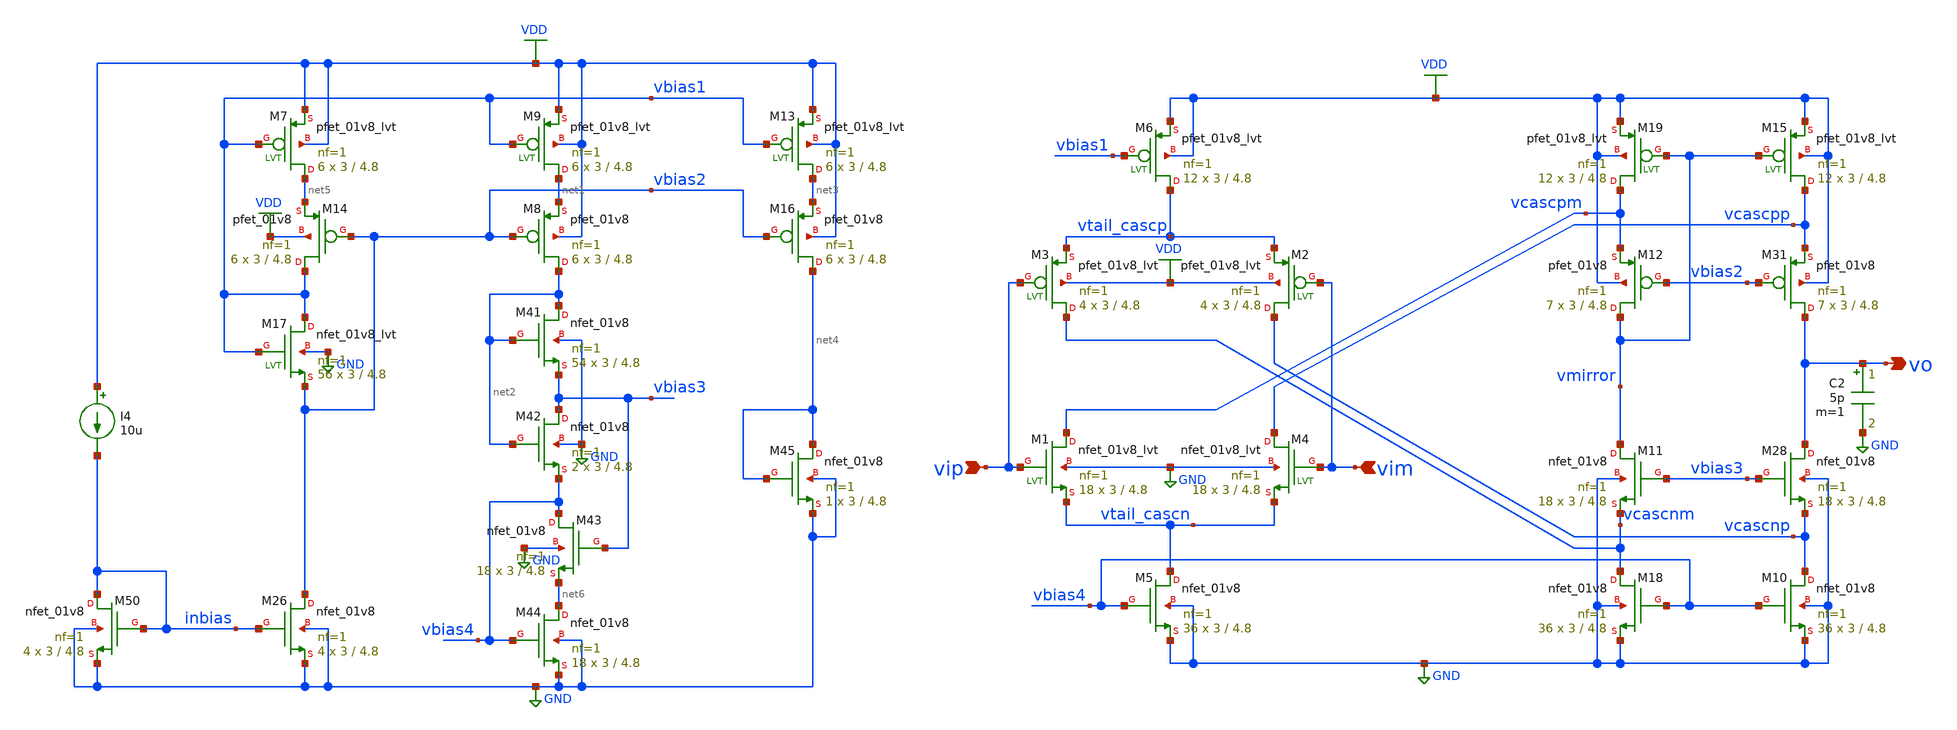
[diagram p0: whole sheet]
** sch_path: designs/se_fold_casc_wide_swing_ota_final.sch
* Copyright 2020 Stefan Frederik Schippers
* Licensed under the Apache License, Version 2.0 (the "License");
* you may not use this file except in compliance with the License.
* You may obtain a copy of the License at
* https://www.apache.org/licenses/LICENSE-2.0
* Unless required by applicable law or agreed to in writing, software
* distributed under the License is distributed on an "AS IS" BASIS,
* WITHOUT WARRANTIES OR CONDITIONS OF ANY KIND, either express or implied.
* See the License for the specific language governing permissions and
* limitations under the License.
**.subckt se_fold_casc_wide_swing_ota_final vip vim vo
*.ipin vip
*.ipin vim
*.opin vo
XM11 vmirror vbias3 vcascnm GND sky130_fd_pr__nfet_01v8 L=4.8 W=3 nf=1 ad='int((nf+1)/2) * W/nf * 0.29'
+ as='int((nf+2)/2) * W/nf * 0.29' pd='2*int((nf+1)/2) * (W/nf + 0.29)' ps='2*int((nf+2)/2) * (W/nf + 0.29)'
+ nrd='0.29 / W' nrs='0.29 / W' sa=0 sb=0 sd=0 mult=18 m=18
XM28 vo vbias3 vcascnp GND sky130_fd_pr__nfet_01v8 L=4.8 W=3 nf=1 ad='int((nf+1)/2) * W/nf * 0.29' as='int((nf+2)/2) * W/nf * 0.29'
+ pd='2*int((nf+1)/2) * (W/nf + 0.29)' ps='2*int((nf+2)/2) * (W/nf + 0.29)' nrd='0.29 / W' nrs='0.29 / W'
+ sa=0 sb=0 sd=0 mult=18 m=18
XM12 vmirror vbias2 vcascpm VDD sky130_fd_pr__pfet_01v8 L=4.8 W=3 nf=1 ad='int((nf+1)/2) * W/nf * 0.29'
+ as='int((nf+2)/2) * W/nf * 0.29' pd='2*int((nf+1)/2) * (W/nf + 0.29)' ps='2*int((nf+2)/2) * (W/nf + 0.29)'
+ nrd='0.29 / W' nrs='0.29 / W' sa=0 sb=0 sd=0 mult=7 m=7
XM31 vo vbias2 vcascpp VDD sky130_fd_pr__pfet_01v8 L=4.8 W=3 nf=1 ad='int((nf+1)/2) * W/nf * 0.29' as='int((nf+2)/2) * W/nf * 0.29'
+ pd='2*int((nf+1)/2) * (W/nf + 0.29)' ps='2*int((nf+2)/2) * (W/nf + 0.29)' nrd='0.29 / W' nrs='0.29 / W'
+ sa=0 sb=0 sd=0 mult=7 m=7
XM5 vtail_cascn vbias4 GND GND sky130_fd_pr__nfet_01v8 L=4.8 W=3 nf=1 ad='int((nf+1)/2) * W/nf * 0.29'
+ as='int((nf+2)/2) * W/nf * 0.29' pd='2*int((nf+1)/2) * (W/nf + 0.29)' ps='2*int((nf+2)/2) * (W/nf + 0.29)'
+ nrd='0.29 / W' nrs='0.29 / W' sa=0 sb=0 sd=0 mult=36 m=36
XM6 vtail_cascp vbias1 VDD VDD sky130_fd_pr__pfet_01v8_lvt L=4.8 W=3 nf=1 ad='int((nf+1)/2) * W/nf * 0.29'
+ as='int((nf+2)/2) * W/nf * 0.29' pd='2*int((nf+1)/2) * (W/nf + 0.29)' ps='2*int((nf+2)/2) * (W/nf + 0.29)'
+ nrd='0.29 / W' nrs='0.29 / W' sa=0 sb=0 sd=0 mult=12 m=12
XM3 vcascnm vip vtail_cascp VDD sky130_fd_pr__pfet_01v8_lvt L=4.8 W=3 nf=1 ad='int((nf+1)/2) * W/nf * 0.29'
+ as='int((nf+2)/2) * W/nf * 0.29' pd='2*int((nf+1)/2) * (W/nf + 0.29)' ps='2*int((nf+2)/2) * (W/nf + 0.29)'
+ nrd='0.29 / W' nrs='0.29 / W' sa=0 sb=0 sd=0 mult=4 m=4
C2 vo GND 5p m=1
XM1 vcascpm vip vtail_cascn GND sky130_fd_pr__nfet_01v8_lvt L=4.8 W=3 nf=1 ad='int((nf+1)/2) * W/nf * 0.29'
+ as='int((nf+2)/2) * W/nf * 0.29' pd='2*int((nf+1)/2) * (W/nf + 0.29)' ps='2*int((nf+2)/2) * (W/nf + 0.29)'
+ nrd='0.29 / W' nrs='0.29 / W' sa=0 sb=0 sd=0 mult=18 m=18
I4 VDD inbias 10u
XM50 inbias inbias GND GND sky130_fd_pr__nfet_01v8 L=4.8 W=3 nf=1 ad='int((nf+1)/2) * W/nf * 0.29' as='int((nf+2)/2) * W/nf * 0.29'
+ pd='2*int((nf+1)/2) * (W/nf + 0.29)' ps='2*int((nf+2)/2) * (W/nf + 0.29)' nrd='0.29 / W' nrs='0.29 / W'
+ sa=0 sb=0 sd=0 mult=4 m=4
XM41 net2 net2 vbias3 GND sky130_fd_pr__nfet_01v8 L=4.8 W=3 nf=1 ad='int((nf+1)/2) * W/nf * 0.29' as='int((nf+2)/2) * W/nf * 0.29'
+ pd='2*int((nf+1)/2) * (W/nf + 0.29)' ps='2*int((nf+2)/2) * (W/nf + 0.29)' nrd='0.29 / W' nrs='0.29 / W'
+ sa=0 sb=0 sd=0 mult=54 m=54
XM42 vbias3 net2 vbias4 GND sky130_fd_pr__nfet_01v8 L=4.8 W=3 nf=1 ad='int((nf+1)/2) * W/nf * 0.29' as='int((nf+2)/2) * W/nf * 0.29'
+ pd='2*int((nf+1)/2) * (W/nf + 0.29)' ps='2*int((nf+2)/2) * (W/nf + 0.29)' nrd='0.29 / W' nrs='0.29 / W'
+ sa=0 sb=0 sd=0 mult=2 m=2
XM43 vbias4 vbias3 net6 GND sky130_fd_pr__nfet_01v8 L=4.8 W=3 nf=1 ad='int((nf+1)/2) * W/nf * 0.29' as='int((nf+2)/2) * W/nf * 0.29'
+ pd='2*int((nf+1)/2) * (W/nf + 0.29)' ps='2*int((nf+2)/2) * (W/nf + 0.29)' nrd='0.29 / W' nrs='0.29 / W'
+ sa=0 sb=0 sd=0 mult=18 m=18
XM44 net6 vbias4 GND GND sky130_fd_pr__nfet_01v8 L=4.8 W=3 nf=1 ad='int((nf+1)/2) * W/nf * 0.29' as='int((nf+2)/2) * W/nf * 0.29'
+ pd='2*int((nf+1)/2) * (W/nf + 0.29)' ps='2*int((nf+2)/2) * (W/nf + 0.29)' nrd='0.29 / W' nrs='0.29 / W'
+ sa=0 sb=0 sd=0 mult=18 m=18
XM45 net4 net4 GND GND sky130_fd_pr__nfet_01v8 L=4.8 W=3 nf=1 ad='int((nf+1)/2) * W/nf * 0.29' as='int((nf+2)/2) * W/nf * 0.29'
+ pd='2*int((nf+1)/2) * (W/nf + 0.29)' ps='2*int((nf+2)/2) * (W/nf + 0.29)' nrd='0.29 / W' nrs='0.29 / W'
+ sa=0 sb=0 sd=0 mult=1 m=1
XM7 net5 vbias1 VDD VDD sky130_fd_pr__pfet_01v8_lvt L=4.8 W=3 nf=1 ad='int((nf+1)/2) * W/nf * 0.29' as='int((nf+2)/2) * W/nf * 0.29'
+ pd='2*int((nf+1)/2) * (W/nf + 0.29)' ps='2*int((nf+2)/2) * (W/nf + 0.29)' nrd='0.29 / W' nrs='0.29 / W'
+ sa=0 sb=0 sd=0 mult=6 m=6
XM8 net2 vbias2 net1 VDD sky130_fd_pr__pfet_01v8 L=4.8 W=3 nf=1 ad='int((nf+1)/2) * W/nf * 0.29' as='int((nf+2)/2) * W/nf * 0.29'
+ pd='2*int((nf+1)/2) * (W/nf + 0.29)' ps='2*int((nf+2)/2) * (W/nf + 0.29)' nrd='0.29 / W' nrs='0.29 / W'
+ sa=0 sb=0 sd=0 mult=6 m=6
XM9 net1 vbias1 VDD VDD sky130_fd_pr__pfet_01v8_lvt L=4.8 W=3 nf=1 ad='int((nf+1)/2) * W/nf * 0.29' as='int((nf+2)/2) * W/nf * 0.29'
+ pd='2*int((nf+1)/2) * (W/nf + 0.29)' ps='2*int((nf+2)/2) * (W/nf + 0.29)' nrd='0.29 / W' nrs='0.29 / W'
+ sa=0 sb=0 sd=0 mult=6 m=6
XM13 net3 vbias1 VDD VDD sky130_fd_pr__pfet_01v8_lvt L=4.8 W=3 nf=1 ad='int((nf+1)/2) * W/nf * 0.29'
+ as='int((nf+2)/2) * W/nf * 0.29' pd='2*int((nf+1)/2) * (W/nf + 0.29)' ps='2*int((nf+2)/2) * (W/nf + 0.29)'
+ nrd='0.29 / W' nrs='0.29 / W' sa=0 sb=0 sd=0 mult=6 m=6
XM14 vbias1 vbias2 net5 VDD sky130_fd_pr__pfet_01v8 L=4.8 W=3 nf=1 ad='int((nf+1)/2) * W/nf * 0.29' as='int((nf+2)/2) * W/nf * 0.29'
+ pd='2*int((nf+1)/2) * (W/nf + 0.29)' ps='2*int((nf+2)/2) * (W/nf + 0.29)' nrd='0.29 / W' nrs='0.29 / W'
+ sa=0 sb=0 sd=0 mult=6 m=6
XM16 net4 vbias2 net3 VDD sky130_fd_pr__pfet_01v8 L=4.8 W=3 nf=1 ad='int((nf+1)/2) * W/nf * 0.29' as='int((nf+2)/2) * W/nf * 0.29'
+ pd='2*int((nf+1)/2) * (W/nf + 0.29)' ps='2*int((nf+2)/2) * (W/nf + 0.29)' nrd='0.29 / W' nrs='0.29 / W'
+ sa=0 sb=0 sd=0 mult=6 m=6
XM26 vbias2 inbias GND GND sky130_fd_pr__nfet_01v8 L=4.8 W=3 nf=1 ad='int((nf+1)/2) * W/nf * 0.29' as='int((nf+2)/2) * W/nf * 0.29'
+ pd='2*int((nf+1)/2) * (W/nf + 0.29)' ps='2*int((nf+2)/2) * (W/nf + 0.29)' nrd='0.29 / W' nrs='0.29 / W'
+ sa=0 sb=0 sd=0 mult=4 m=4
XM17 vbias1 vbias1 vbias2 GND sky130_fd_pr__nfet_01v8_lvt L=4.8 W=3 nf=1 ad='int((nf+1)/2) * W/nf * 0.29'
+ as='int((nf+2)/2) * W/nf * 0.29' pd='2*int((nf+1)/2) * (W/nf + 0.29)' ps='2*int((nf+2)/2) * (W/nf + 0.29)'
+ nrd='0.29 / W' nrs='0.29 / W' sa=0 sb=0 sd=0 mult=56 m=56
XM10 vcascnp vbias4 GND GND sky130_fd_pr__nfet_01v8 L=4.8 W=3 nf=1 ad='int((nf+1)/2) * W/nf * 0.29' as='int((nf+2)/2) * W/nf * 0.29'
+ pd='2*int((nf+1)/2) * (W/nf + 0.29)' ps='2*int((nf+2)/2) * (W/nf + 0.29)' nrd='0.29 / W' nrs='0.29 / W'
+ sa=0 sb=0 sd=0 mult=36 m=36
XM18 vcascnm vbias4 GND GND sky130_fd_pr__nfet_01v8 L=4.8 W=3 nf=1 ad='int((nf+1)/2) * W/nf * 0.29' as='int((nf+2)/2) * W/nf * 0.29'
+ pd='2*int((nf+1)/2) * (W/nf + 0.29)' ps='2*int((nf+2)/2) * (W/nf + 0.29)' nrd='0.29 / W' nrs='0.29 / W'
+ sa=0 sb=0 sd=0 mult=36 m=36
XM4 vcascpp vim vtail_cascn GND sky130_fd_pr__nfet_01v8_lvt L=4.8 W=3 nf=1 ad='int((nf+1)/2) * W/nf * 0.29'
+ as='int((nf+2)/2) * W/nf * 0.29' pd='2*int((nf+1)/2) * (W/nf + 0.29)' ps='2*int((nf+2)/2) * (W/nf + 0.29)'
+ nrd='0.29 / W' nrs='0.29 / W' sa=0 sb=0 sd=0 mult=18 m=18
XM2 vcascnp vim vtail_cascp VDD sky130_fd_pr__pfet_01v8_lvt L=4.8 W=3 nf=1 ad='int((nf+1)/2) * W/nf * 0.29'
+ as='int((nf+2)/2) * W/nf * 0.29' pd='2*int((nf+1)/2) * (W/nf + 0.29)' ps='2*int((nf+2)/2) * (W/nf + 0.29)'
+ nrd='0.29 / W' nrs='0.29 / W' sa=0 sb=0 sd=0 mult=4 m=4
XM15 vcascpp vmirror VDD VDD sky130_fd_pr__pfet_01v8_lvt L=4.8 W=3 nf=1 ad='int((nf+1)/2) * W/nf * 0.29'
+ as='int((nf+2)/2) * W/nf * 0.29' pd='2*int((nf+1)/2) * (W/nf + 0.29)' ps='2*int((nf+2)/2) * (W/nf + 0.29)'
+ nrd='0.29 / W' nrs='0.29 / W' sa=0 sb=0 sd=0 mult=12 m=12
XM19 vcascpm vmirror VDD VDD sky130_fd_pr__pfet_01v8_lvt L=4.8 W=3 nf=1 ad='int((nf+1)/2) * W/nf * 0.29'
+ as='int((nf+2)/2) * W/nf * 0.29' pd='2*int((nf+1)/2) * (W/nf + 0.29)' ps='2*int((nf+2)/2) * (W/nf + 0.29)'
+ nrd='0.29 / W' nrs='0.29 / W' sa=0 sb=0 sd=0 mult=12 m=12
**** begin user architecture code

.include $::SKYWATER_MODELS/cells/nfet_01v8/sky130_fd_pr__nfet_01v8__tt.corner.spice
.include $::SKYWATER_MODELS/cells/nfet_01v8_lvt/sky130_fd_pr__nfet_01v8_lvt__tt.corner.spice
.include $::SKYWATER_MODELS/cells/pfet_01v8/sky130_fd_pr__pfet_01v8__tt.corner.spice
.include $::SKYWATER_MODELS/cells/nfet_03v3_nvt/sky130_fd_pr__nfet_03v3_nvt__tt.corner.spice
.include $::SKYWATER_MODELS/cells/nfet_05v0_nvt/sky130_fd_pr__nfet_05v0_nvt__tt.corner.spice
.include $::SKYWATER_MODELS/cells/esd_nfet_01v8/sky130_fd_pr__esd_nfet_01v8__tt.corner.spice
.include $::SKYWATER_MODELS/cells/pfet_01v8_lvt/sky130_fd_pr__pfet_01v8_lvt__tt.corner.spice
.include $::SKYWATER_MODELS/cells/pfet_01v8_hvt/sky130_fd_pr__pfet_01v8_hvt__tt.corner.spice
.include $::SKYWATER_MODELS/cells/esd_pfet_g5v0d10v5/sky130_fd_pr__esd_pfet_g5v0d10v5__tt.corner.spice
.include $::SKYWATER_MODELS/cells/pfet_g5v0d10v5/sky130_fd_pr__pfet_g5v0d10v5__tt.corner.spice
.include $::SKYWATER_MODELS/cells/pfet_g5v0d16v0/sky130_fd_pr__pfet_g5v0d16v0__tt.corner.spice
.include $::SKYWATER_MODELS/cells/nfet_g5v0d10v5/sky130_fd_pr__nfet_g5v0d10v5__tt.corner.spice
.include $::SKYWATER_MODELS/cells/nfet_g5v0d16v0/sky130_fd_pr__nfet_g5v0d16v0__tt_discrete.corner.spice
.include $::SKYWATER_MODELS/cells/esd_nfet_g5v0d10v5/sky130_fd_pr__esd_nfet_g5v0d10v5__tt.corner.spice
.include $::SKYWATER_MODELS/models/corners/tt/nonfet.spice
* Mismatch parameters
.include $::SKYWATER_MODELS/cells/nfet_01v8/sky130_fd_pr__nfet_01v8__mismatch.corner.spice
.include $::SKYWATER_MODELS/cells/pfet_01v8/sky130_fd_pr__pfet_01v8__mismatch.corner.spice
.include $::SKYWATER_MODELS/cells/nfet_01v8_lvt/sky130_fd_pr__nfet_01v8_lvt__mismatch.corner.spice
.include $::SKYWATER_MODELS/cells/pfet_01v8_lvt/sky130_fd_pr__pfet_01v8_lvt__mismatch.corner.spice
.include $::SKYWATER_MODELS/cells/pfet_01v8_hvt/sky130_fd_pr__pfet_01v8_hvt__mismatch.corner.spice
.include $::SKYWATER_MODELS/cells/nfet_g5v0d10v5/sky130_fd_pr__nfet_g5v0d10v5__mismatch.corner.spice
.include $::SKYWATER_MODELS/cells/pfet_g5v0d10v5/sky130_fd_pr__pfet_g5v0d10v5__mismatch.corner.spice
.include $::SKYWATER_MODELS/cells/nfet_05v0_nvt/sky130_fd_pr__nfet_05v0_nvt__mismatch.corner.spice
.include $::SKYWATER_MODELS/cells/nfet_03v3_nvt/sky130_fd_pr__nfet_03v3_nvt__mismatch.corner.spice
* Resistor$::SKYWATER_MODELS/Capacitor
.include $::SKYWATER_MODELS/models/r+c/res_typical__cap_typical.spice
.include $::SKYWATER_MODELS/models/r+c/res_typical__cap_typical__lin.spice
* Special cells
.include $::SKYWATER_MODELS/models/corners/tt/specialized_cells.spice
* All models
.include $::SKYWATER_MODELS/models/all.spice
* Corner
.include $::SKYWATER_MODELS/models/corners/tt/rf.spice

**** end user architecture code
**.ends
.GLOBAL GND
.GLOBAL VDD
**** begin user architecture code

.include se_fold_casc_wide_swing_ota_final_commands.spice

**** end user architecture code
.end
